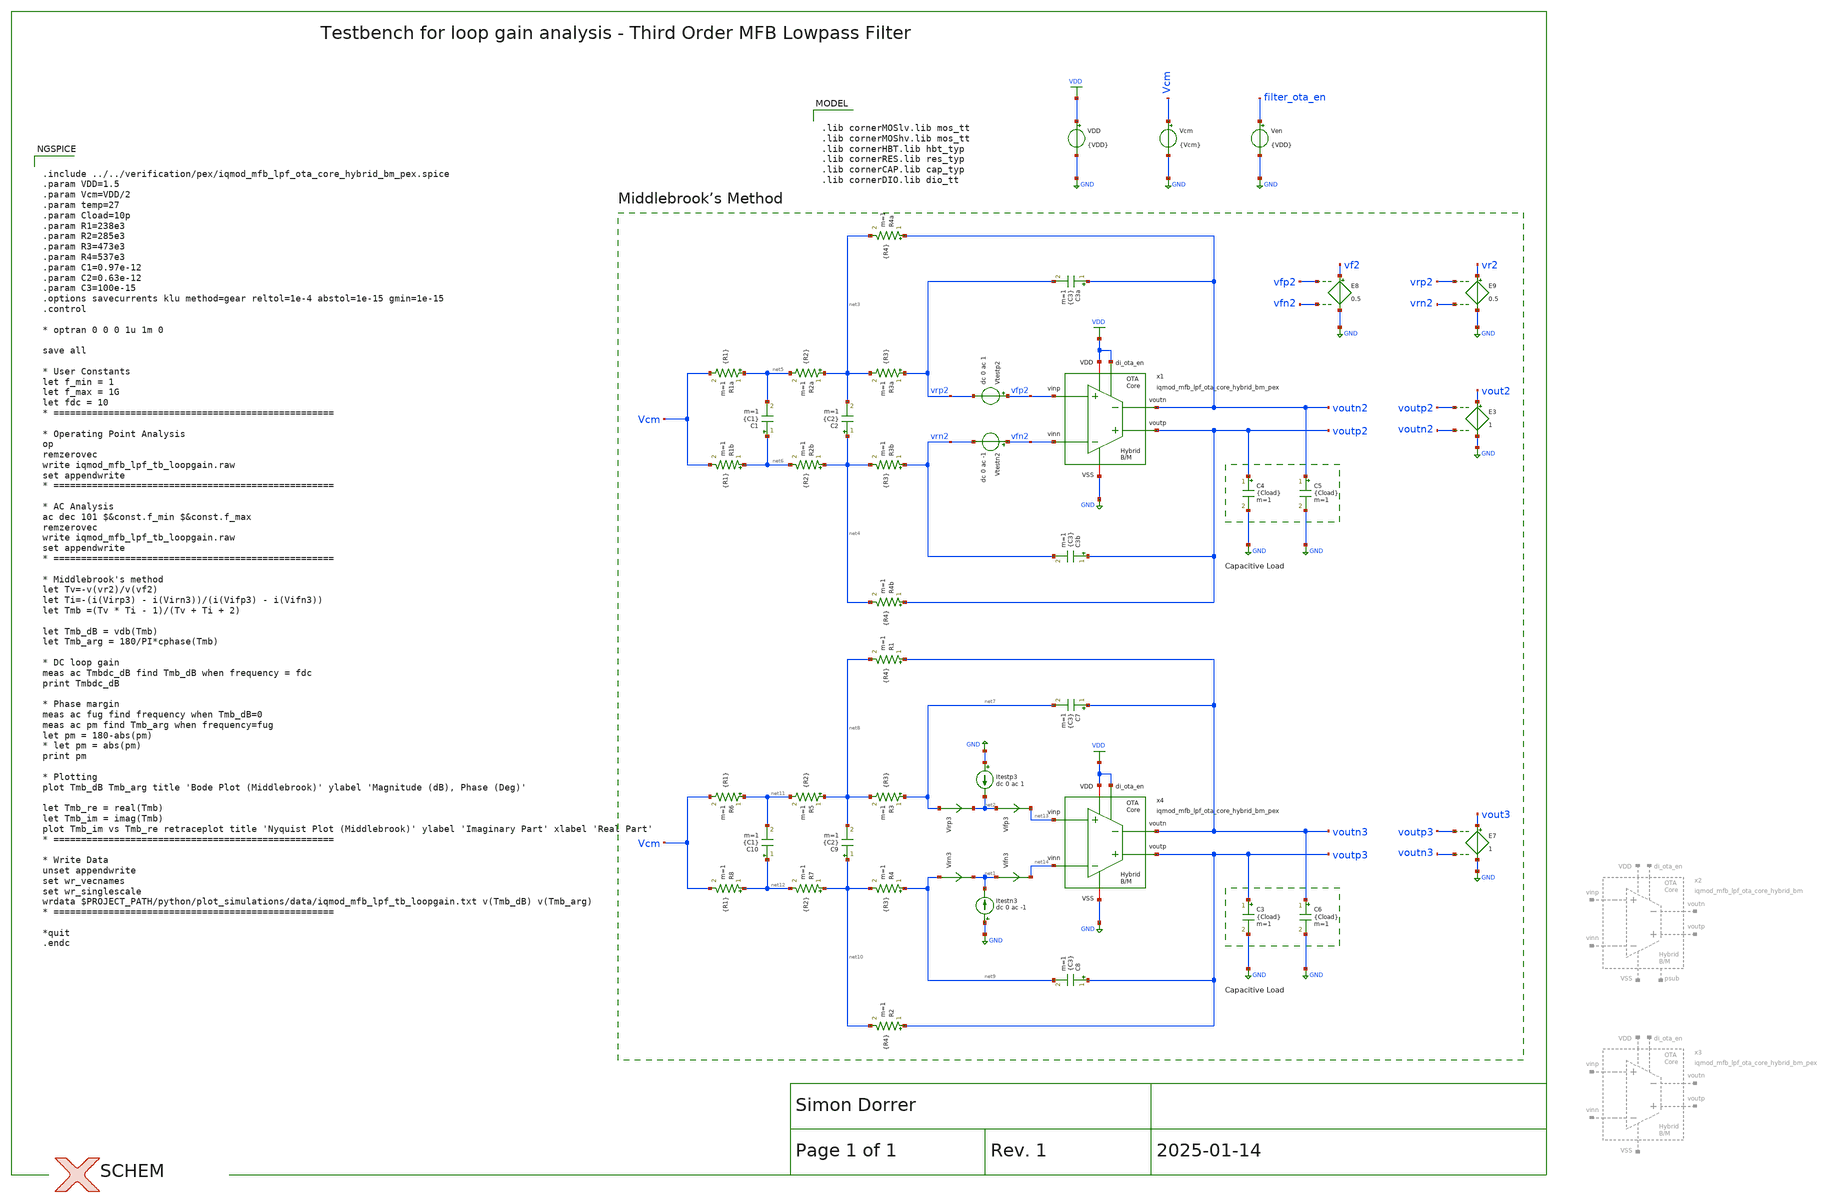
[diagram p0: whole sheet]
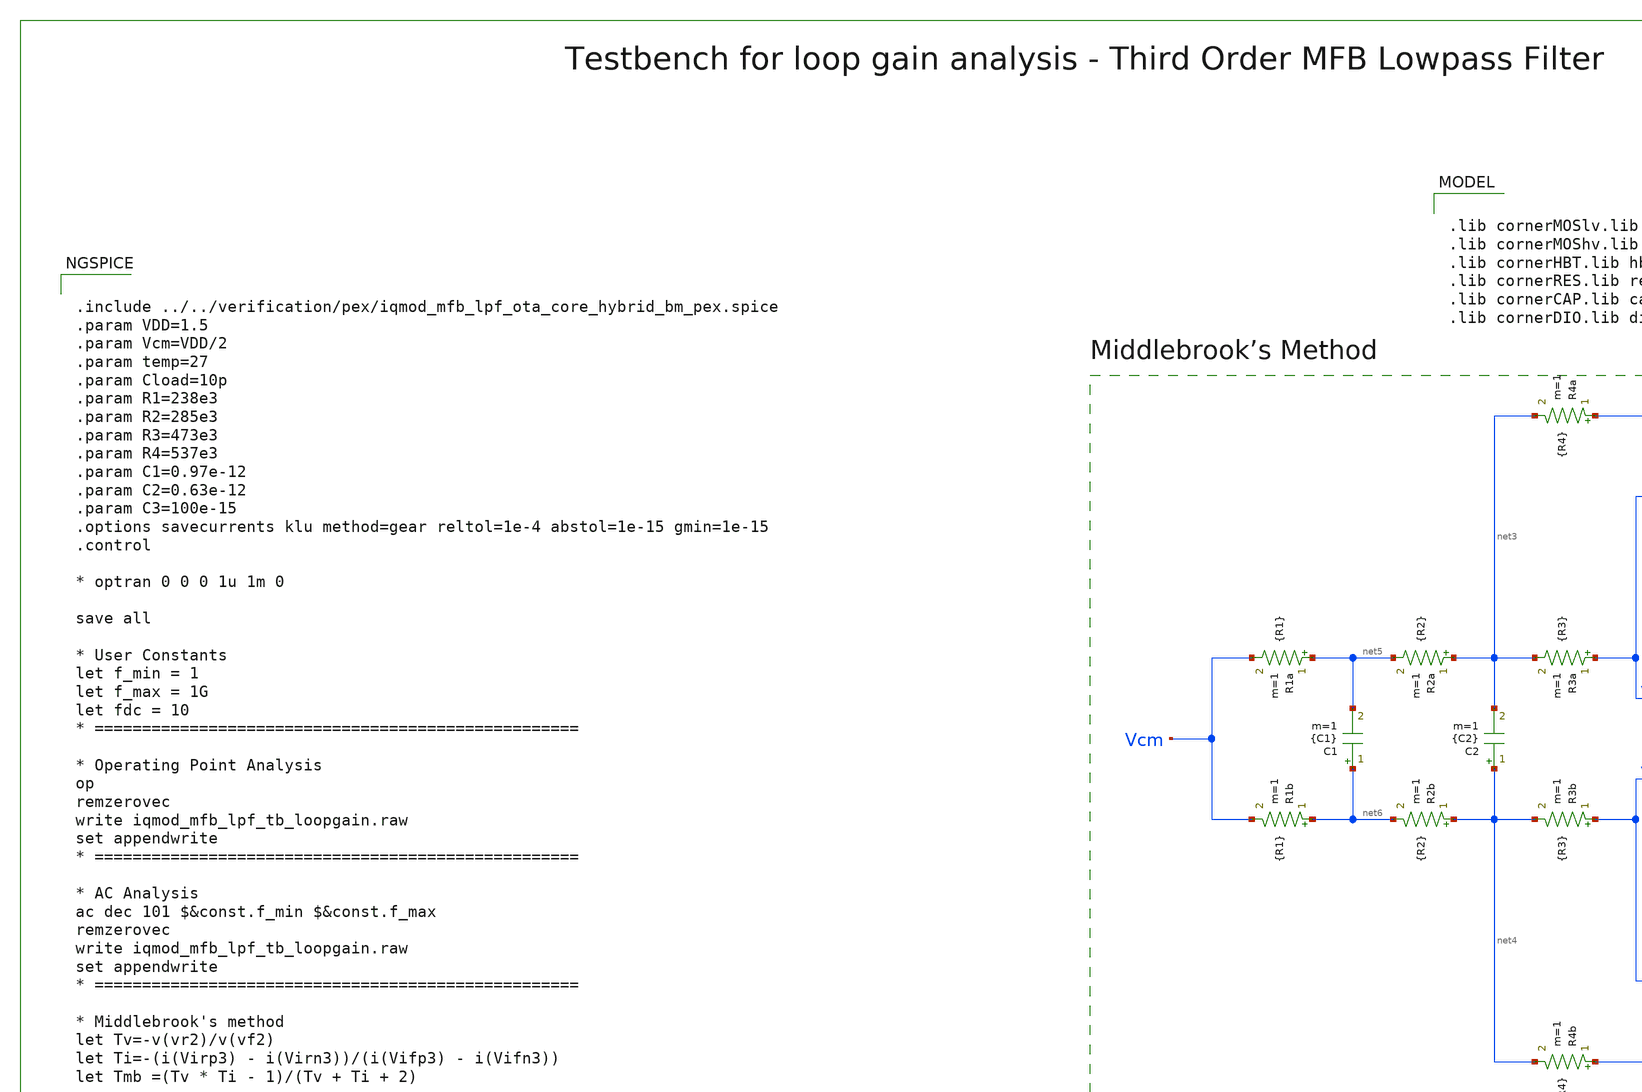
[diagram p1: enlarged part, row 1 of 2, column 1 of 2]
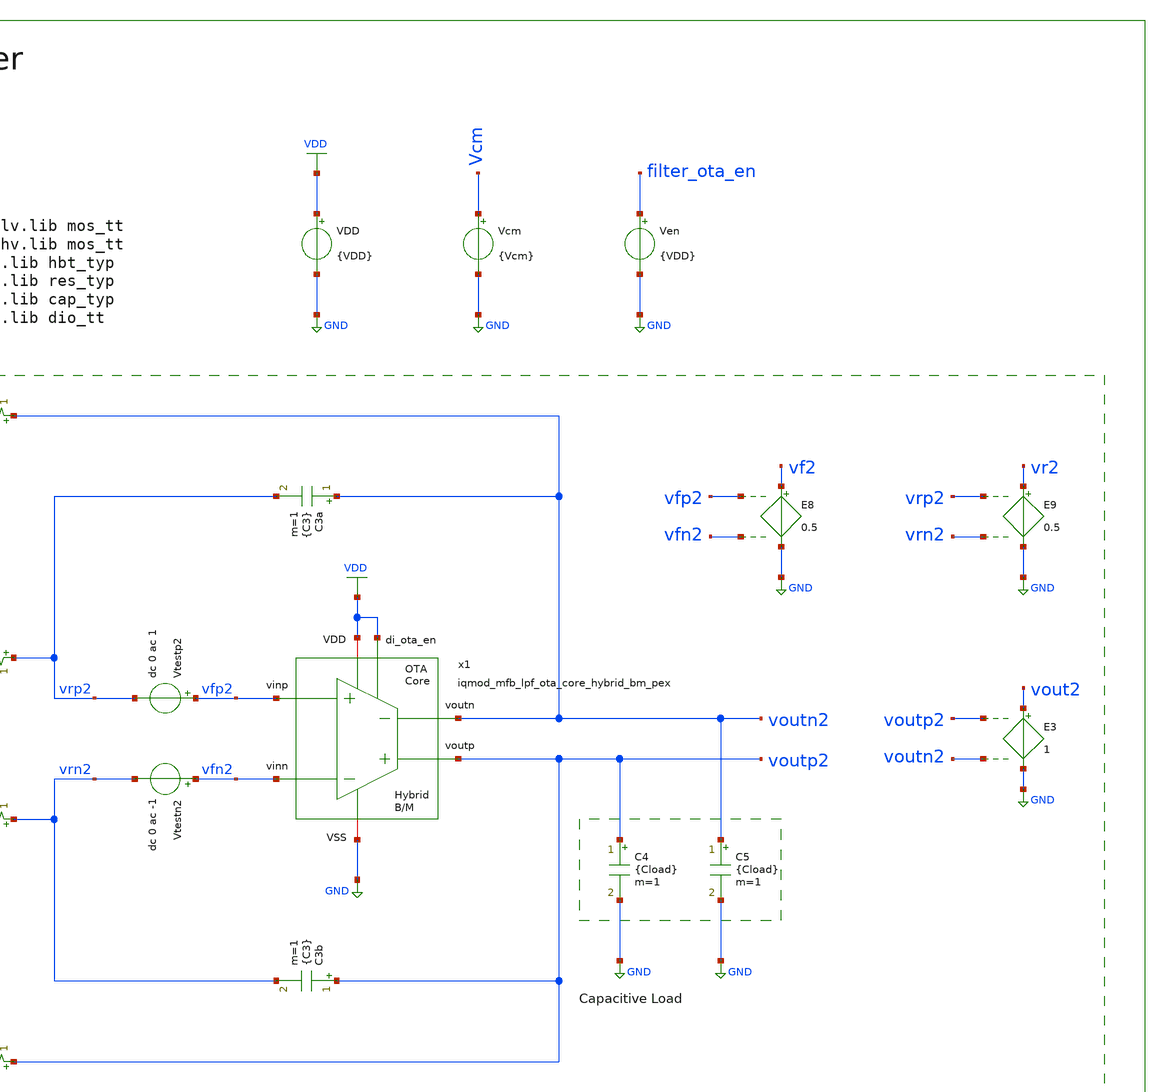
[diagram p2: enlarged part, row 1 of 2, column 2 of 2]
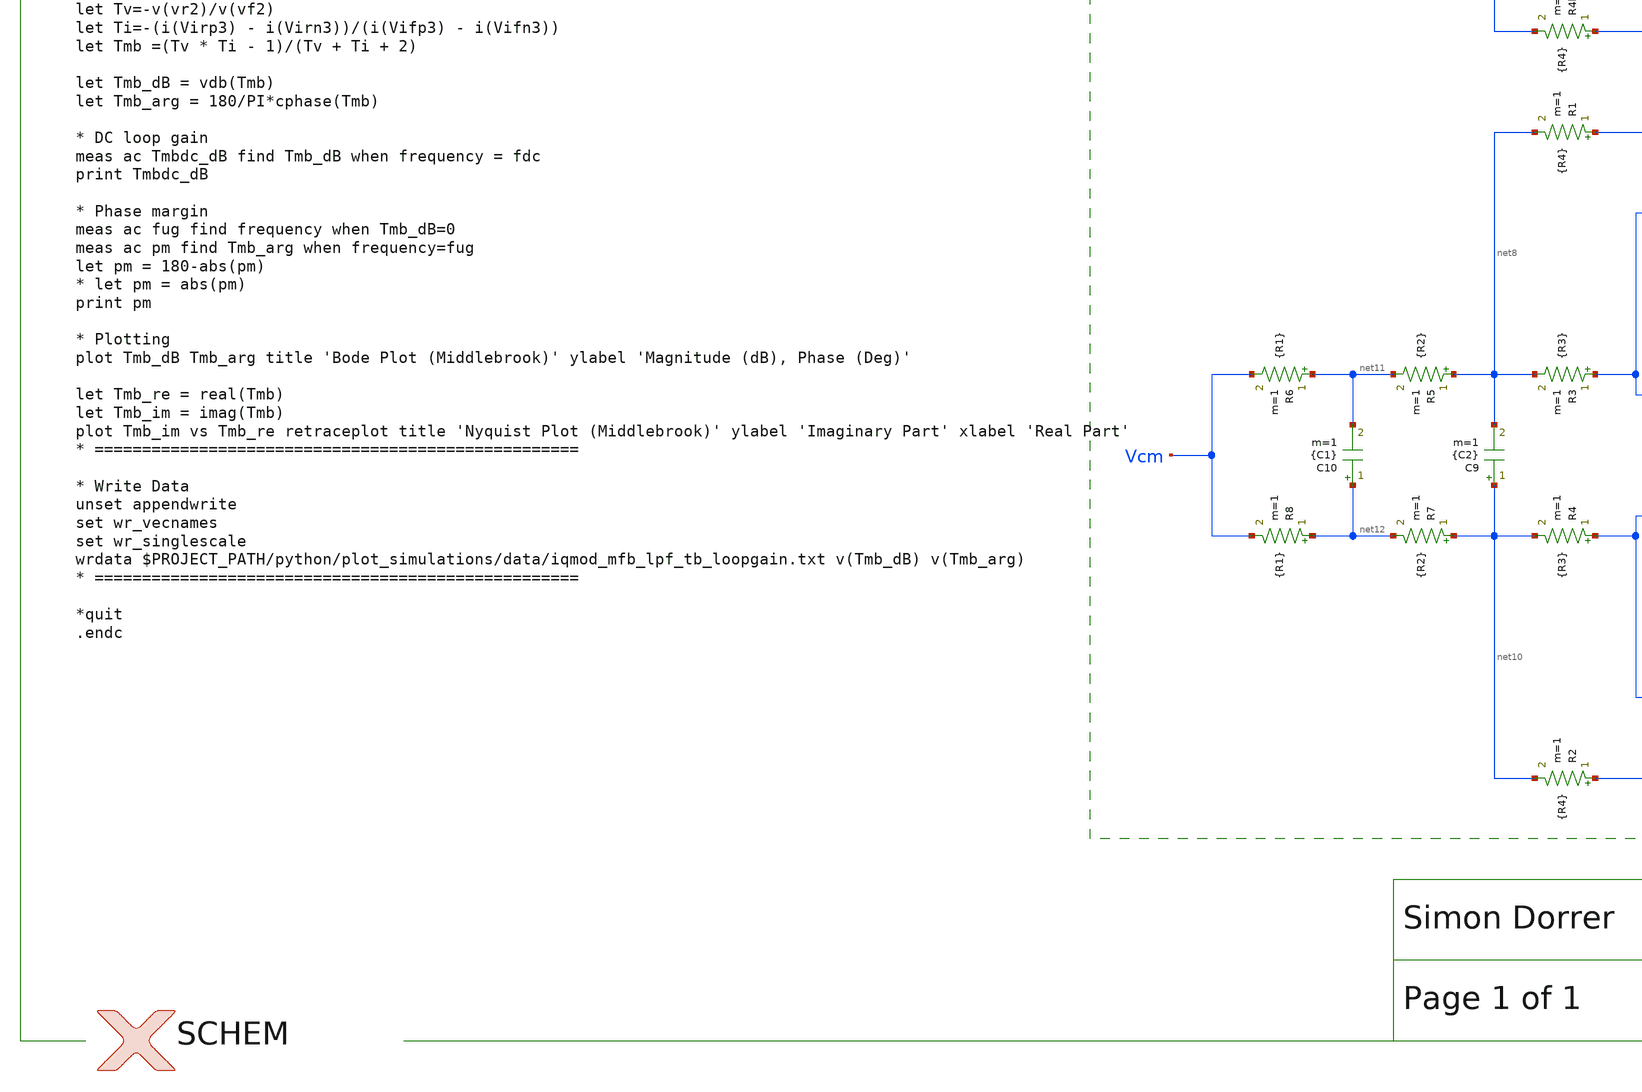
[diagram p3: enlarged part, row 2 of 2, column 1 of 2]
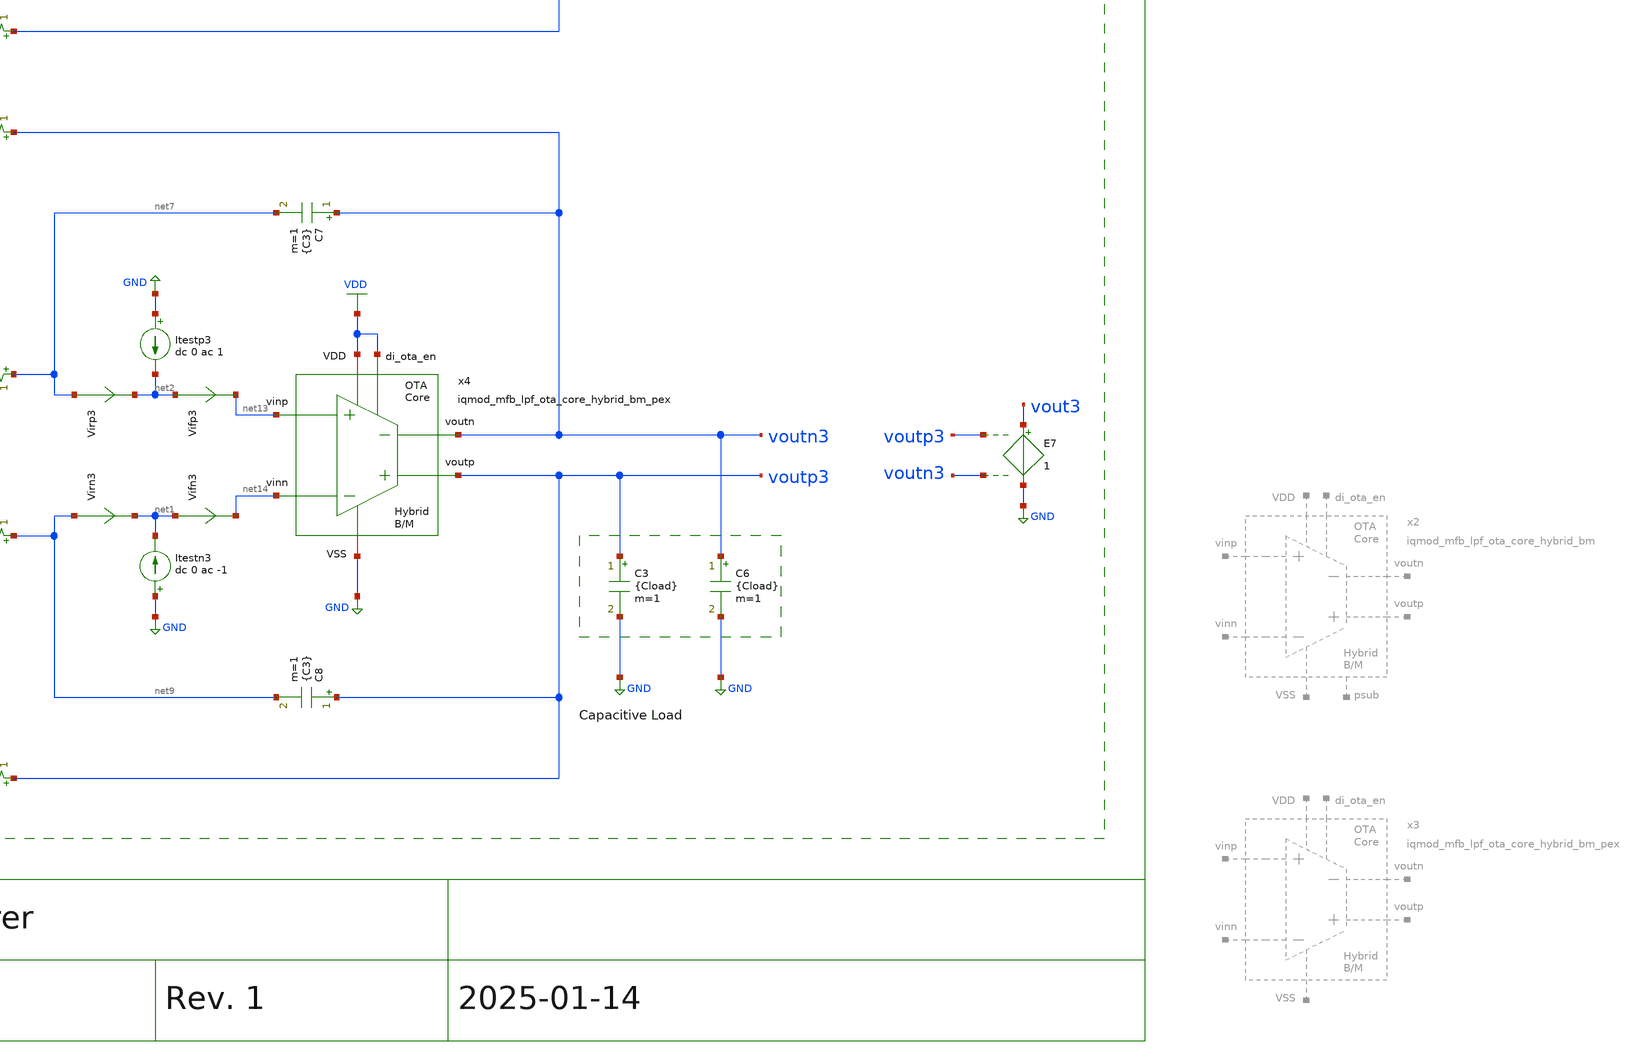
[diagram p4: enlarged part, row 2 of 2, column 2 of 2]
** sch_path: ihp130/macros/iqmod/xschem/testbenches/iqmod_mfb_lpf_tb_loopgain.sch
**.subckt iqmod_mfb_lpf_tb_loopgain
VDD VDD GND {VDD}
Ven filter_ota_en GND {VDD}
C4 voutp2 GND {Cload} m=1
C5 voutn2 GND {Cload} m=1
E3 vout2 GND voutp2 voutn2 1
R4a voutn2 net3 {R4} m=1
R4b voutp2 net4 {R4} m=1
C3a voutn2 vrp2 {C3} m=1
C3b voutp2 vrn2 {C3} m=1
C2 net4 net3 {C2} m=1
E7 vout3 GND voutp3 voutn3 1
E8 vf2 GND vfp2 vfn2 0.5
E9 vr2 GND vrp2 vrn2 0.5
Vtestp2 vfp2 vrp2 dc 0 ac 1
Vtestn2 vfn2 vrn2 dc 0 ac -1
Virp3 net7 net2 0
.save i(virp3)
Vifp3 net2 net13 0
.save i(vifp3)
Itestn3 GND net1 dc 0 ac -1
Virn3 net9 net1 0
.save i(virn3)
Vifn3 net1 net14 0
.save i(vifn3)
Itestp3 GND net2 dc 0 ac 1
Vcm Vcm GND {Vcm}
R3a vrp2 net3 {R3} m=1
R3b vrn2 net4 {R3} m=1
R2a net3 net5 {R2} m=1
R1a net5 Vcm {R1} m=1
R2b net4 net6 {R2} m=1
R1b net6 Vcm {R1} m=1
C1 net6 net5 {C1} m=1
C3 voutp3 GND {Cload} m=1
C6 voutn3 GND {Cload} m=1
R1 voutn3 net8 {R4} m=1
R2 voutp3 net10 {R4} m=1
C7 voutn3 net7 {C3} m=1
C8 voutp3 net9 {C3} m=1
C9 net10 net8 {C2} m=1
R3 net7 net8 {R3} m=1
R4 net9 net10 {R3} m=1
R5 net8 net11 {R2} m=1
R6 net11 Vcm {R1} m=1
R7 net10 net12 {R2} m=1
R8 net12 Vcm {R1} m=1
C10 net12 net11 {C1} m=1
x1 voutp2 voutn2 vfn2 vfp2 VDD GND VDD iqmod_mfb_lpf_ota_core_hybrid_bm_pex
x4 voutp3 voutn3 net14 net13 VDD GND VDD iqmod_mfb_lpf_ota_core_hybrid_bm_pex
**** begin user architecture code


.include ../../verification/pex/iqmod_mfb_lpf_ota_core_hybrid_bm_pex.spice
.param VDD=1.5
.param Vcm=VDD/2
.param temp=27
.param Cload=10p
.param R1=238e3
.param R2=285e3
.param R3=473e3
.param R4=537e3
.param C1=0.97e-12
.param C2=0.63e-12
.param C3=100e-15
.options savecurrents klu method=gear reltol=1e-4 abstol=1e-15 gmin=1e-15
.control

* optran 0 0 0 1u 1m 0

save all

* User Constants
let f_min = 1
let f_max = 1G
let fdc = 10
* ===================================================

* Operating Point Analysis
op
remzerovec
write iqmod_mfb_lpf_tb_loopgain.raw
set appendwrite
* ===================================================

* AC Analysis
ac dec 101 $&const.f_min $&const.f_max
remzerovec
write iqmod_mfb_lpf_tb_loopgain.raw
set appendwrite
* ===================================================

* Middlebrook's method
let Tv=-v(vr2)/v(vf2)
let Ti=-(i(Virp3) - i(Virn3))/(i(Vifp3) - i(Vifn3))
let Tmb =(Tv * Ti - 1)/(Tv + Ti + 2)

let Tmb_dB = vdb(Tmb)
let Tmb_arg = 180/PI*cphase(Tmb)

* DC loop gain
meas ac Tmbdc_dB find Tmb_dB when frequency = fdc
print Tmbdc_dB

* Phase margin
meas ac fug find frequency when Tmb_dB=0
meas ac pm find Tmb_arg when frequency=fug
let pm = 180-abs(pm)
* let pm = abs(pm)
print pm

* Plotting
plot Tmb_dB Tmb_arg title 'Bode Plot (Middlebrook)' ylabel 'Magnitude (dB), Phase (Deg)'

let Tmb_re = real(Tmb)
let Tmb_im = imag(Tmb)
plot Tmb_im vs Tmb_re retraceplot title 'Nyquist Plot (Middlebrook)' ylabel 'Imaginary Part' xlabel 'Real
+ Part'
* ===================================================

* Write Data
unset appendwrite
set wr_vecnames
set wr_singlescale
wrdata $PROJECT_PATH/python/plot_simulations/data/iqmod_mfb_lpf_tb_loopgain.txt v(Tmb_dB) v(Tmb_arg)
* ===================================================

*quit
.endc



.lib cornerMOSlv.lib mos_tt
.lib cornerMOShv.lib mos_tt
.lib cornerHBT.lib hbt_typ
.lib cornerRES.lib res_typ
.lib cornerCAP.lib cap_typ
.lib cornerDIO.lib dio_tt

**** end user architecture code
**.ends
.GLOBAL GND
.GLOBAL VDD
.end
